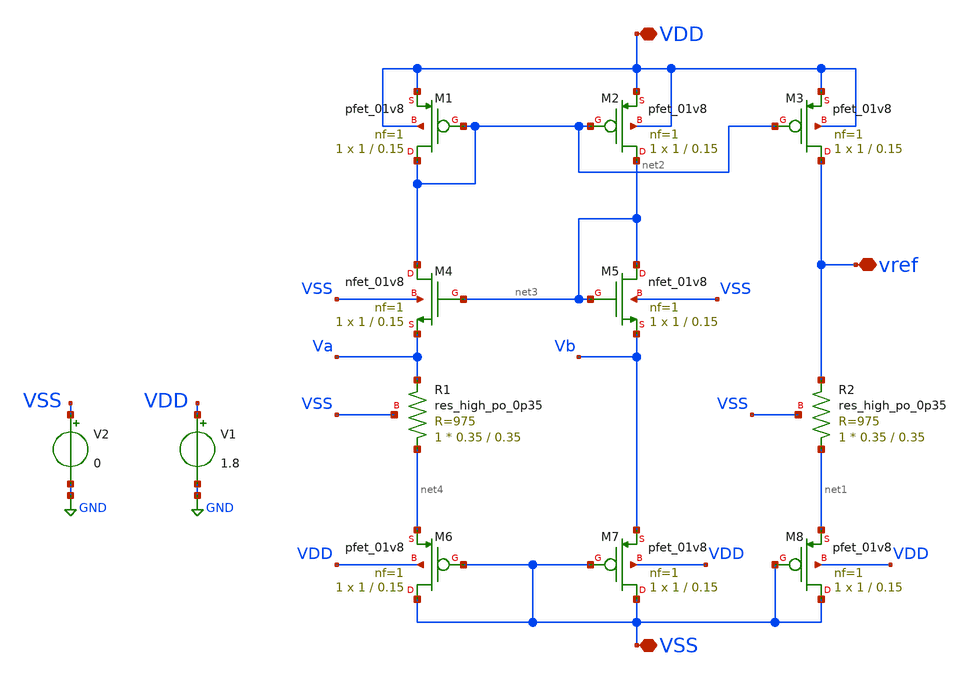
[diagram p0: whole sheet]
** sch_path: xschem/bandgap.sch
**.subckt bandgap VSS VDD vref
*.iopin VSS
*.iopin VDD
*.iopin vref
XM1 net2 net2 VDD VDD sky130_fd_pr__pfet_01v8 L=0.15 W=1 nf=1 ad='int((nf+1)/2) * W/nf * 0.29' as='int((nf+2)/2) * W/nf * 0.29'
+ pd='2*int((nf+1)/2) * (W/nf + 0.29)' ps='2*int((nf+2)/2) * (W/nf + 0.29)' nrd='0.29 / W' nrs='0.29 / W'
+ sa=0 sb=0 sd=0 mult=1 m=1
XM2 net3 net2 VDD VDD sky130_fd_pr__pfet_01v8 L=0.15 W=1 nf=1 ad='int((nf+1)/2) * W/nf * 0.29' as='int((nf+2)/2) * W/nf * 0.29'
+ pd='2*int((nf+1)/2) * (W/nf + 0.29)' ps='2*int((nf+2)/2) * (W/nf + 0.29)' nrd='0.29 / W' nrs='0.29 / W'
+ sa=0 sb=0 sd=0 mult=1 m=1
XM3 vref net2 VDD VDD sky130_fd_pr__pfet_01v8 L=0.15 W=1 nf=1 ad='int((nf+1)/2) * W/nf * 0.29' as='int((nf+2)/2) * W/nf * 0.29'
+ pd='2*int((nf+1)/2) * (W/nf + 0.29)' ps='2*int((nf+2)/2) * (W/nf + 0.29)' nrd='0.29 / W' nrs='0.29 / W'
+ sa=0 sb=0 sd=0 mult=1 m=1
XM4 net2 net3 Va VSS sky130_fd_pr__nfet_01v8 L=0.15 W=1 nf=1 ad='int((nf+1)/2) * W/nf * 0.29' as='int((nf+2)/2) * W/nf * 0.29'
+ pd='2*int((nf+1)/2) * (W/nf + 0.29)' ps='2*int((nf+2)/2) * (W/nf + 0.29)' nrd='0.29 / W' nrs='0.29 / W'
+ sa=0 sb=0 sd=0 mult=1 m=1
XM5 net3 net3 Vb VSS sky130_fd_pr__nfet_01v8 L=0.15 W=1 nf=1 ad='int((nf+1)/2) * W/nf * 0.29' as='int((nf+2)/2) * W/nf * 0.29'
+ pd='2*int((nf+1)/2) * (W/nf + 0.29)' ps='2*int((nf+2)/2) * (W/nf + 0.29)' nrd='0.29 / W' nrs='0.29 / W'
+ sa=0 sb=0 sd=0 mult=1 m=1
XM6 VSS VSS net4 VDD sky130_fd_pr__pfet_01v8 L=0.15 W=1 nf=1 ad='int((nf+1)/2) * W/nf * 0.29' as='int((nf+2)/2) * W/nf * 0.29'
+ pd='2*int((nf+1)/2) * (W/nf + 0.29)' ps='2*int((nf+2)/2) * (W/nf + 0.29)' nrd='0.29 / W' nrs='0.29 / W'
+ sa=0 sb=0 sd=0 mult=1 m=1
XM7 VSS VSS Vb VDD sky130_fd_pr__pfet_01v8 L=0.15 W=1 nf=1 ad='int((nf+1)/2) * W/nf * 0.29' as='int((nf+2)/2) * W/nf * 0.29'
+ pd='2*int((nf+1)/2) * (W/nf + 0.29)' ps='2*int((nf+2)/2) * (W/nf + 0.29)' nrd='0.29 / W' nrs='0.29 / W'
+ sa=0 sb=0 sd=0 mult=1 m=1
XM8 VSS VSS net1 VDD sky130_fd_pr__pfet_01v8 L=0.15 W=1 nf=1 ad='int((nf+1)/2) * W/nf * 0.29' as='int((nf+2)/2) * W/nf * 0.29'
+ pd='2*int((nf+1)/2) * (W/nf + 0.29)' ps='2*int((nf+2)/2) * (W/nf + 0.29)' nrd='0.29 / W' nrs='0.29 / W'
+ sa=0 sb=0 sd=0 mult=1 m=1
XR1 net4 Va VSS sky130_fd_pr__res_high_po_0p35 L=0.35 mult=1 m=1
XR2 net1 vref VSS sky130_fd_pr__res_high_po_0p35 L=0.35 mult=1 m=1
V1 VDD GND 1.8
V2 VSS GND 0
**** begin user architecture code

** opencircuitdesign pdks install
.lib $::SKYWATER_MODELS/sky130.lib.spice tt





*.option  METHOD = GEAR
*.param mc_mm_switch=0
.control
let tempv = 10            ; create a vector vddc and assign 1.8
repeat 20
  set temp = $&tempv         ; alter the voltage V1 using vector vddc
  tran 500p 1u uic
  let tempv = tempv + 5   ; update vddc
  write bandgap.raw
  set appendwrite
  reset
end
.endc



**** end user architecture code
**.ends
.GLOBAL GND
.end
